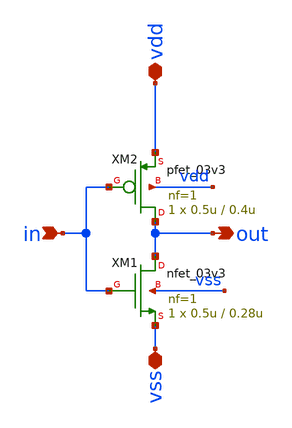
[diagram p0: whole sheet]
** sch_path: General/ADC/OTA/inverter.sch
**.subckt inverter vdd vss in out
*.iopin vdd
*.iopin vss
*.ipin in
*.opin out
XM1 out in vss vss nfet_03v3 L=0.28u W=0.5u nf=1 ad='int((nf+1)/2) * W/nf * 0.18u' as='int((nf+2)/2) * W/nf * 0.18u'
+ pd='2*int((nf+1)/2) * (W/nf + 0.18u)' ps='2*int((nf+2)/2) * (W/nf + 0.18u)' nrd='0.18u / W' nrs='0.18u / W'
+ sa=0 sb=0 sd=0 m=1
XM2 out in vdd vdd pfet_03v3 L=0.4u W=0.5u nf=1 ad='int((nf+1)/2) * W/nf * 0.18u' as='int((nf+2)/2) * W/nf * 0.18u'
+ pd='2*int((nf+1)/2) * (W/nf + 0.18u)' ps='2*int((nf+2)/2) * (W/nf + 0.18u)' nrd='0.18u / W' nrs='0.18u / W'
+ sa=0 sb=0 sd=0 m=1
**.ends
.end
